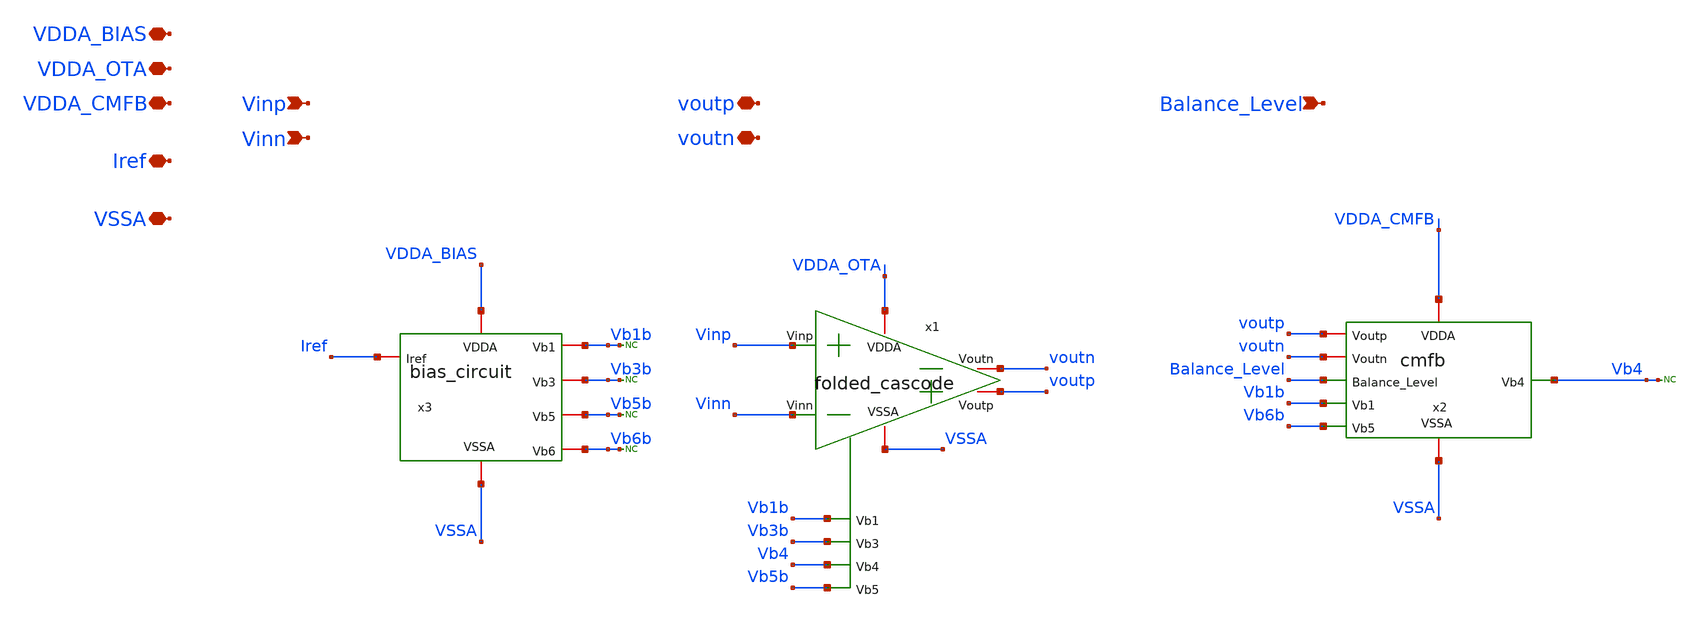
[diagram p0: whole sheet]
** sch_path: Folded_cascode/schematic/top_fc_power.sch
**.subckt top_fc_power Iref VDDA_CMFB VSSA Vinp Vinn Balance_Level voutp voutn VDDA_OTA VDDA_BIAS
*.iopin Iref
*.iopin VDDA_CMFB
*.iopin VSSA
*.ipin Vinp
*.ipin Vinn
*.ipin Balance_Level
*.iopin voutp
*.iopin voutn
*.iopin VDDA_OTA
*.iopin VDDA_BIAS
x2 VDDA_CMFB VSSA voutp voutn Balance_Level Vb1b Vb4 Vb6b cmfb
* noconn Vb3b
* noconn Vb5b
* noconn Vb1b
* noconn Vb6b
x3 VDDA_BIAS Vb3b Vb1b Vb5b VSSA Iref Vb6b bias_circuit
* noconn Vb4
x1 VDDA_OTA VSSA Vinp Vinn voutp voutn Vb1b Vb3b Vb4 Vb5b folded_cascode
**.ends
.end
